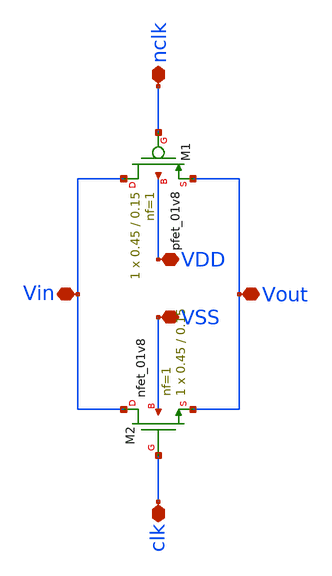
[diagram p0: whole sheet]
** sch_path: TT/tgate.sch
**.subckt tgate nclk clk VDD VSS Vout Vin
*.iopin nclk
*.iopin clk
*.iopin VDD
*.iopin VSS
*.iopin Vout
*.iopin Vin
XM1 Vin nclk Vout VDD sky130_fd_pr__pfet_01v8 L=0.15 W=0.45 nf=1 ad='int((nf+1)/2) * W/nf * 0.29' as='int((nf+2)/2) * W/nf * 0.29'
+ pd='2*int((nf+1)/2) * (W/nf + 0.29)' ps='2*int((nf+2)/2) * (W/nf + 0.29)' nrd='0.29 / W' nrs='0.29 / W'
+ sa=0 sb=0 sd=0 mult=1 m=1
XM2 Vin clk Vout VSS sky130_fd_pr__nfet_01v8 L=0.15 W=0.45 nf=1 ad='int((nf+1)/2) * W/nf * 0.29' as='int((nf+2)/2) * W/nf * 0.29'
+ pd='2*int((nf+1)/2) * (W/nf + 0.29)' ps='2*int((nf+2)/2) * (W/nf + 0.29)' nrd='0.29 / W' nrs='0.29 / W'
+ sa=0 sb=0 sd=0 mult=1 m=1
**.ends
.end
